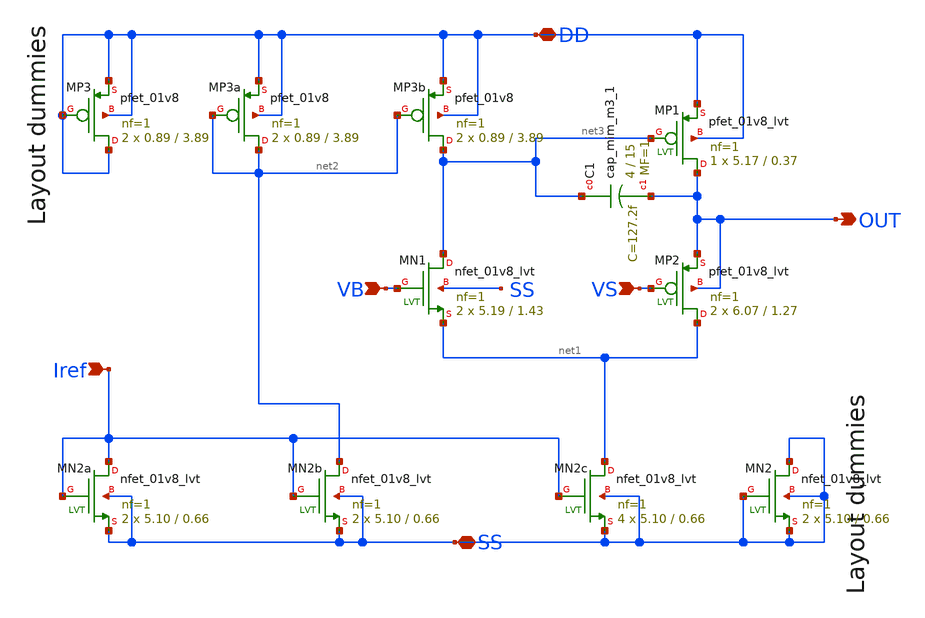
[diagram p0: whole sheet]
** sch_path: xschem/ldo.sch
**.subckt ldo DD Iref OUT VB VS SS
*.iopin DD
*.ipin Iref
*.opin OUT
*.ipin VB
*.ipin VS
*.iopin SS
XMN1 net3 VB net1 SS sky130_fd_pr__nfet_01v8_lvt L=1.43 W=5.19 nf=1 ad='int((nf+1)/2) * W/nf * 0.29'
+ as='int((nf+2)/2) * W/nf * 0.29' pd='2*int((nf+1)/2) * (W/nf + 0.29)' ps='2*int((nf+2)/2) * (W/nf + 0.29)'
+ nrd='0.29 / W' nrs='0.29 / W' sa=0 sb=0 sd=0 mult=2 m=2
XMN2c net1 Iref SS SS sky130_fd_pr__nfet_01v8_lvt L=0.66 W=5.10 nf=1 ad='int((nf+1)/2) * W/nf * 0.29'
+ as='int((nf+2)/2) * W/nf * 0.29' pd='2*int((nf+1)/2) * (W/nf + 0.29)' ps='2*int((nf+2)/2) * (W/nf + 0.29)'
+ nrd='0.29 / W' nrs='0.29 / W' sa=0 sb=0 sd=0 mult=4 m=4
XMN2b net2 Iref SS SS sky130_fd_pr__nfet_01v8_lvt L=0.66 W=5.10 nf=1 ad='int((nf+1)/2) * W/nf * 0.29'
+ as='int((nf+2)/2) * W/nf * 0.29' pd='2*int((nf+1)/2) * (W/nf + 0.29)' ps='2*int((nf+2)/2) * (W/nf + 0.29)'
+ nrd='0.29 / W' nrs='0.29 / W' sa=0 sb=0 sd=0 mult=2 m=2
XMN2a Iref Iref SS SS sky130_fd_pr__nfet_01v8_lvt L=0.66 W=5.10 nf=1 ad='int((nf+1)/2) * W/nf * 0.29'
+ as='int((nf+2)/2) * W/nf * 0.29' pd='2*int((nf+1)/2) * (W/nf + 0.29)' ps='2*int((nf+2)/2) * (W/nf + 0.29)'
+ nrd='0.29 / W' nrs='0.29 / W' sa=0 sb=0 sd=0 mult=2 m=2
XMP2 net1 VS OUT OUT sky130_fd_pr__pfet_01v8_lvt L=1.27 W=6.07 nf=1 ad='int((nf+1)/2) * W/nf * 0.29'
+ as='int((nf+2)/2) * W/nf * 0.29' pd='2*int((nf+1)/2) * (W/nf + 0.29)' ps='2*int((nf+2)/2) * (W/nf + 0.29)'
+ nrd='0.29 / W' nrs='0.29 / W' sa=0 sb=0 sd=0 mult=2 m=2
XMP1 OUT net3 DD DD sky130_fd_pr__pfet_01v8_lvt L=0.37 W=5.17 nf=1 ad='int((1 + 1)/2) * 5.17 / 1 * 0.29'
+ as='int((1 + 2)/2) * 5.17 / 1 * 0.29' pd='2*int((1 + 1)/2) * (5.17 / 1 + 0.29)' ps='2*int((1 + 2)/2) * (5.17 / 1 + 0.29)'
+ nrd='0.29 / 5.17 ' nrs='0.29 / 5.17 ' sa=0 sb=0 sd=0 mult=1 m=1
XMP3b net3 net2 DD DD sky130_fd_pr__pfet_01v8 L=3.89 W=0.89 nf=1 ad='int((nf+1)/2) * W/nf * 0.29' as='int((nf+2)/2) * W/nf * 0.29'
+ pd='2*int((nf+1)/2) * (W/nf + 0.29)' ps='2*int((nf+2)/2) * (W/nf + 0.29)' nrd='0.29 / W' nrs='0.29 / W'
+ sa=0 sb=0 sd=0 mult=2 m=2
XMP3a net2 net2 DD DD sky130_fd_pr__pfet_01v8 L=3.89 W=0.89 nf=1 ad='int((nf+1)/2) * W/nf * 0.29' as='int((nf+2)/2) * W/nf * 0.29'
+ pd='2*int((nf+1)/2) * (W/nf + 0.29)' ps='2*int((nf+2)/2) * (W/nf + 0.29)' nrd='0.29 / W' nrs='0.29 / W'
+ sa=0 sb=0 sd=0 mult=2 m=2
XC1 net3 OUT sky130_fd_pr__cap_mim_m3_1 W=4 L=15 MF=1 m=1
XMP3 DD DD DD DD sky130_fd_pr__pfet_01v8 L=3.89 W=0.89 nf=1 ad='int((nf+1)/2) * W/nf * 0.29' as='int((nf+2)/2) * W/nf * 0.29'
+ pd='2*int((nf+1)/2) * (W/nf + 0.29)' ps='2*int((nf+2)/2) * (W/nf + 0.29)' nrd='0.29 / W' nrs='0.29 / W'
+ sa=0 sb=0 sd=0 mult=2 m=2
XMN2 SS SS SS SS sky130_fd_pr__nfet_01v8_lvt L=0.66 W=5.10 nf=1 ad='int((nf+1)/2) * W/nf * 0.29' as='int((nf+2)/2) * W/nf * 0.29'
+ pd='2*int((nf+1)/2) * (W/nf + 0.29)' ps='2*int((nf+2)/2) * (W/nf + 0.29)' nrd='0.29 / W' nrs='0.29 / W'
+ sa=0 sb=0 sd=0 mult=2 m=2
**.ends
.end
